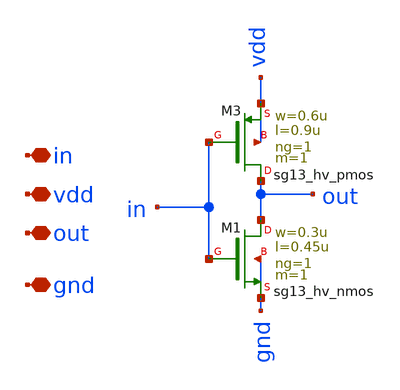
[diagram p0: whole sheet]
** sch_path: dependencies/OTA/OTA-main/schematic/xschem/Clock_gen_using_transistor_hv/inverter.sch
**.subckt inverter in vdd out gnd
*.iopin in
*.iopin vdd
*.iopin out
*.iopin gnd
XM3 out in vdd vdd sg13_hv_pmos w=0.6u l=0.9u ng=1 m=1 mm_ok=1
XM1 out in gnd gnd sg13_hv_nmos w=0.3u l=0.45u ng=1 m=1 mm_ok=1
**.ends
.end
